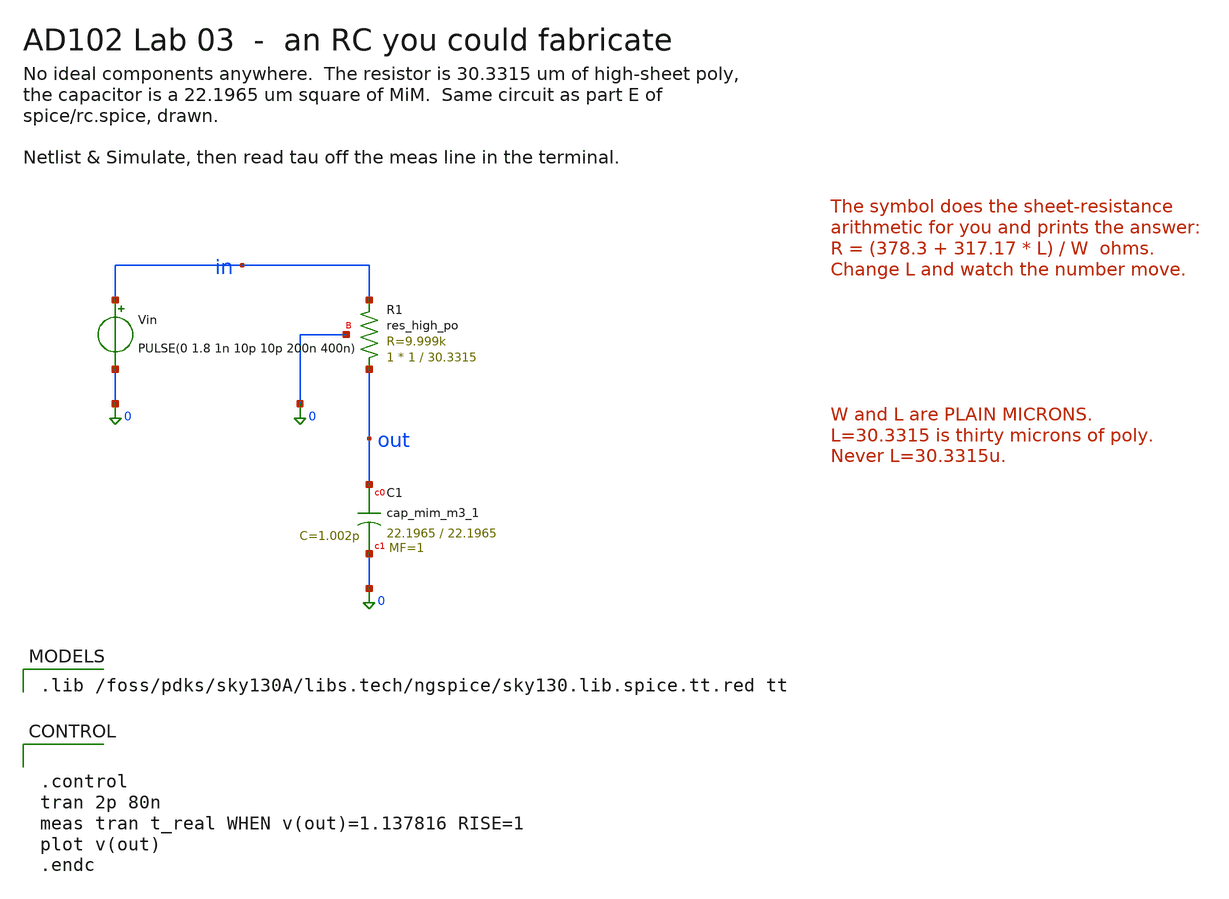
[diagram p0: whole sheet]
** sch_path: labs/lab-03-a-time-constant-in-silicon/xschem/rc.sch
**.subckt rc
XR1 out in 0 sky130_fd_pr__res_high_po W=1 L=30.3315 mult=1 m=1
XC1 out 0 sky130_fd_pr__cap_mim_m3_1 W=22.1965 L=22.1965 MF=1 m=1
Vin in 0 PULSE(0 1.8 1n 10p 10p 200n 400n)
**** begin user architecture code

.lib /foss/pdks/sky130A/libs.tech/ngspice/sky130.lib.spice.tt.red tt



.control
tran 2p 80n
meas tran t_real WHEN v(out)=1.137816 RISE=1
plot v(out)
.endc


**** end user architecture code
**.ends
.end
